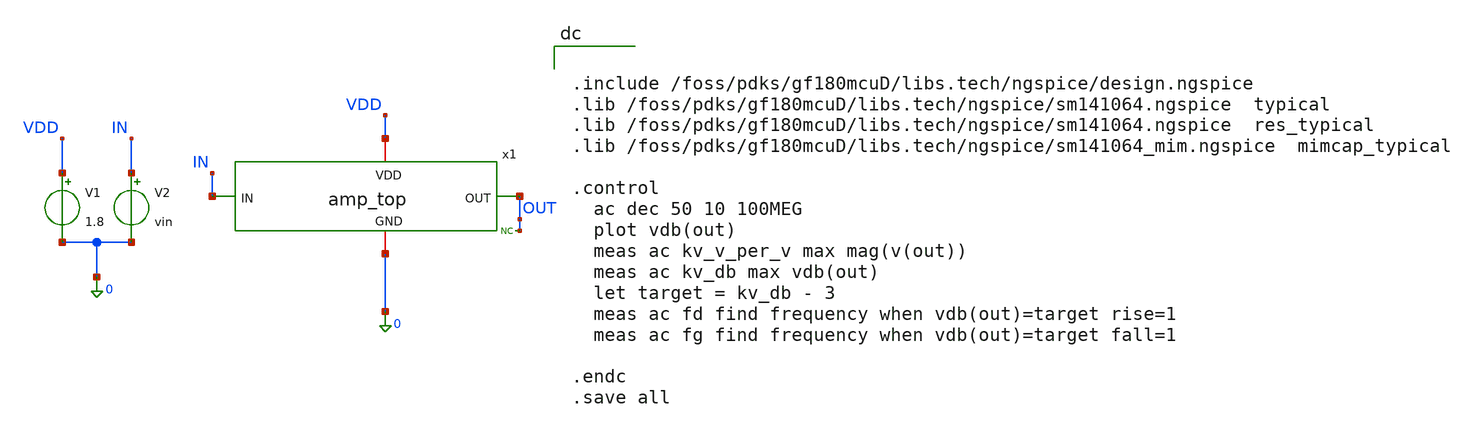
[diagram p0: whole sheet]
** sch_path: amp_top_test.sch
**.subckt amp_top_test
x1 IN OUT VDD 0 amp_top
V1 VDD 0 1.8
V2 IN 0 vin
* noconn OUT
**** begin user architecture code


.include /foss/pdks/gf180mcuD/libs.tech/ngspice/design.ngspice
.lib /foss/pdks/gf180mcuD/libs.tech/ngspice/sm141064.ngspice  typical
.lib /foss/pdks/gf180mcuD/libs.tech/ngspice/sm141064.ngspice  res_typical
.lib /foss/pdks/gf180mcuD/libs.tech/ngspice/sm141064_mim.ngspice  mimcap_typical

.control
  ac dec 50 10 100MEG
  plot vdb(out)
  meas ac kv_v_per_v max mag(v(out))
  meas ac kv_db max vdb(out)
  let target = kv_db - 3
  meas ac fd find frequency when vdb(out)=target rise=1
  meas ac fg find frequency when vdb(out)=target fall=1

.endc
.save all


**** end user architecture code
**.ends
.end
